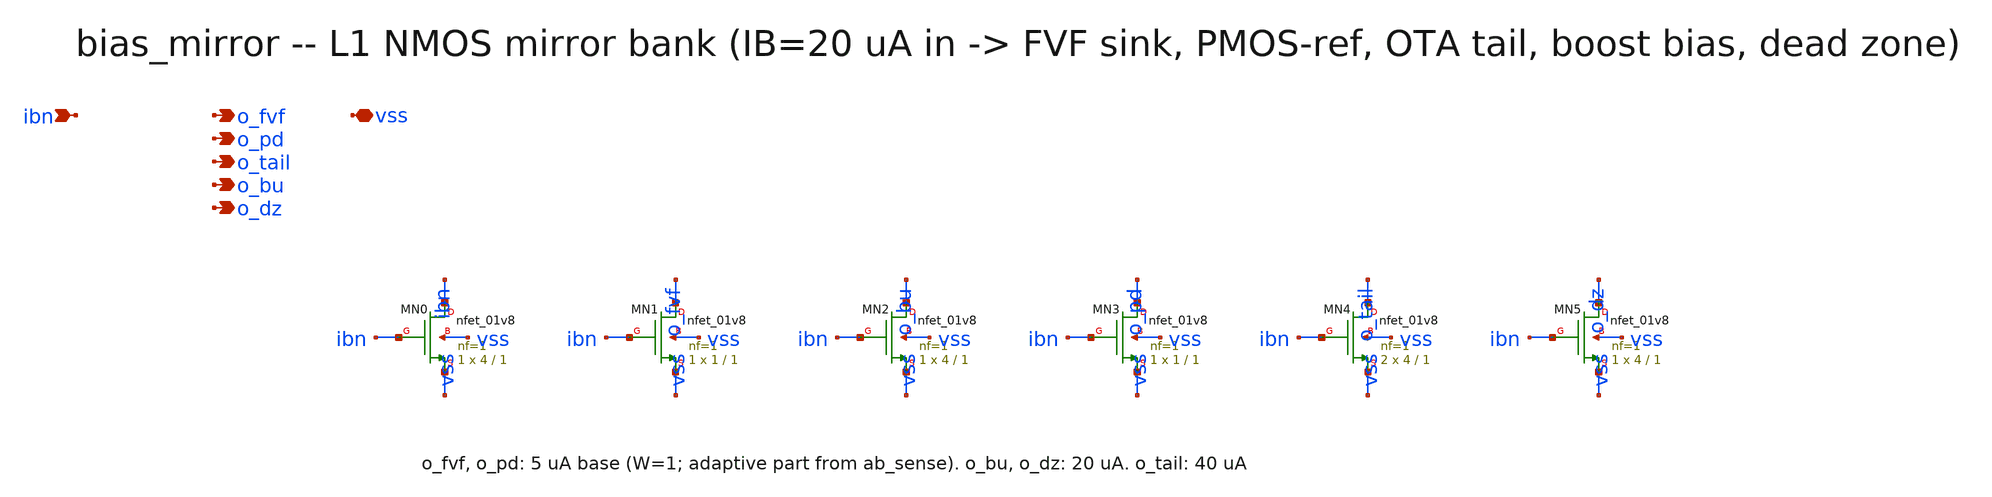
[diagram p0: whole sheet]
** sch_path: xschem/onetops/bias_mirror.sch
**.subckt bias_mirror ibn o_fvf o_pd o_tail o_bu o_dz vss
*.ipin ibn
*.opin o_fvf
*.opin o_pd
*.opin o_tail
*.opin o_bu
*.opin o_dz
*.iopin vss
XMN0 ibn ibn vss vss sky130_fd_pr__nfet_01v8 L=1 W=4 nf=1 ad='int((1 + 1)/2) * 4 / 1 * 0.29' as='int((1 + 2)/2) * 4 / 1 * 0.29'
+ pd='2*int((1 + 1)/2) * (4 / 1 + 0.29)' ps='2*int((1 + 2)/2) * (4 / 1 + 0.29)' nrd='0.29 / 4 ' nrs='0.29 / 4 '
+ sa=0 sb=0 sd=0 mult=1 m=1
XMN1 o_fvf ibn vss vss sky130_fd_pr__nfet_01v8 L=1 W=1 nf=1 ad='int((1 + 1)/2) * 1 / 1 * 0.29' as='int((1 + 2)/2) * 1 / 1 * 0.29'
+ pd='2*int((1 + 1)/2) * (1 / 1 + 0.29)' ps='2*int((1 + 2)/2) * (1 / 1 + 0.29)' nrd='0.29 / 1 ' nrs='0.29 / 1 '
+ sa=0 sb=0 sd=0 mult=1 m=1
XMN2 o_bu ibn vss vss sky130_fd_pr__nfet_01v8 L=1 W=4 nf=1 ad='int((1 + 1)/2) * 4 / 1 * 0.29' as='int((1 + 2)/2) * 4 / 1 * 0.29'
+ pd='2*int((1 + 1)/2) * (4 / 1 + 0.29)' ps='2*int((1 + 2)/2) * (4 / 1 + 0.29)' nrd='0.29 / 4 ' nrs='0.29 / 4 '
+ sa=0 sb=0 sd=0 mult=1 m=1
XMN3 o_pd ibn vss vss sky130_fd_pr__nfet_01v8 L=1 W=1 nf=1 ad='int((1 + 1)/2) * 1 / 1 * 0.29' as='int((1 + 2)/2) * 1 / 1 * 0.29'
+ pd='2*int((1 + 1)/2) * (1 / 1 + 0.29)' ps='2*int((1 + 2)/2) * (1 / 1 + 0.29)' nrd='0.29 / 1 ' nrs='0.29 / 1 '
+ sa=0 sb=0 sd=0 mult=1 m=1
XMN4 o_tail ibn vss vss sky130_fd_pr__nfet_01v8 L=1 W=4 nf=1 ad='int((1 + 1)/2) * 4 / 1 * 0.29' as='int((1 + 2)/2) * 4 / 1 * 0.29'
+ pd='2*int((1 + 1)/2) * (4 / 1 + 0.29)' ps='2*int((1 + 2)/2) * (4 / 1 + 0.29)' nrd='0.29 / 4 ' nrs='0.29 / 4 '
+ sa=0 sb=0 sd=0 mult=2 m=2
XMN5 o_dz ibn vss vss sky130_fd_pr__nfet_01v8 L=1 W=4 nf=1 ad='int((1 + 1)/2) * 4 / 1 * 0.29' as='int((1 + 2)/2) * 4 / 1 * 0.29'
+ pd='2*int((1 + 1)/2) * (4 / 1 + 0.29)' ps='2*int((1 + 2)/2) * (4 / 1 + 0.29)' nrd='0.29 / 4 ' nrs='0.29 / 4 '
+ sa=0 sb=0 sd=0 mult=1 m=1
**.ends
.end
